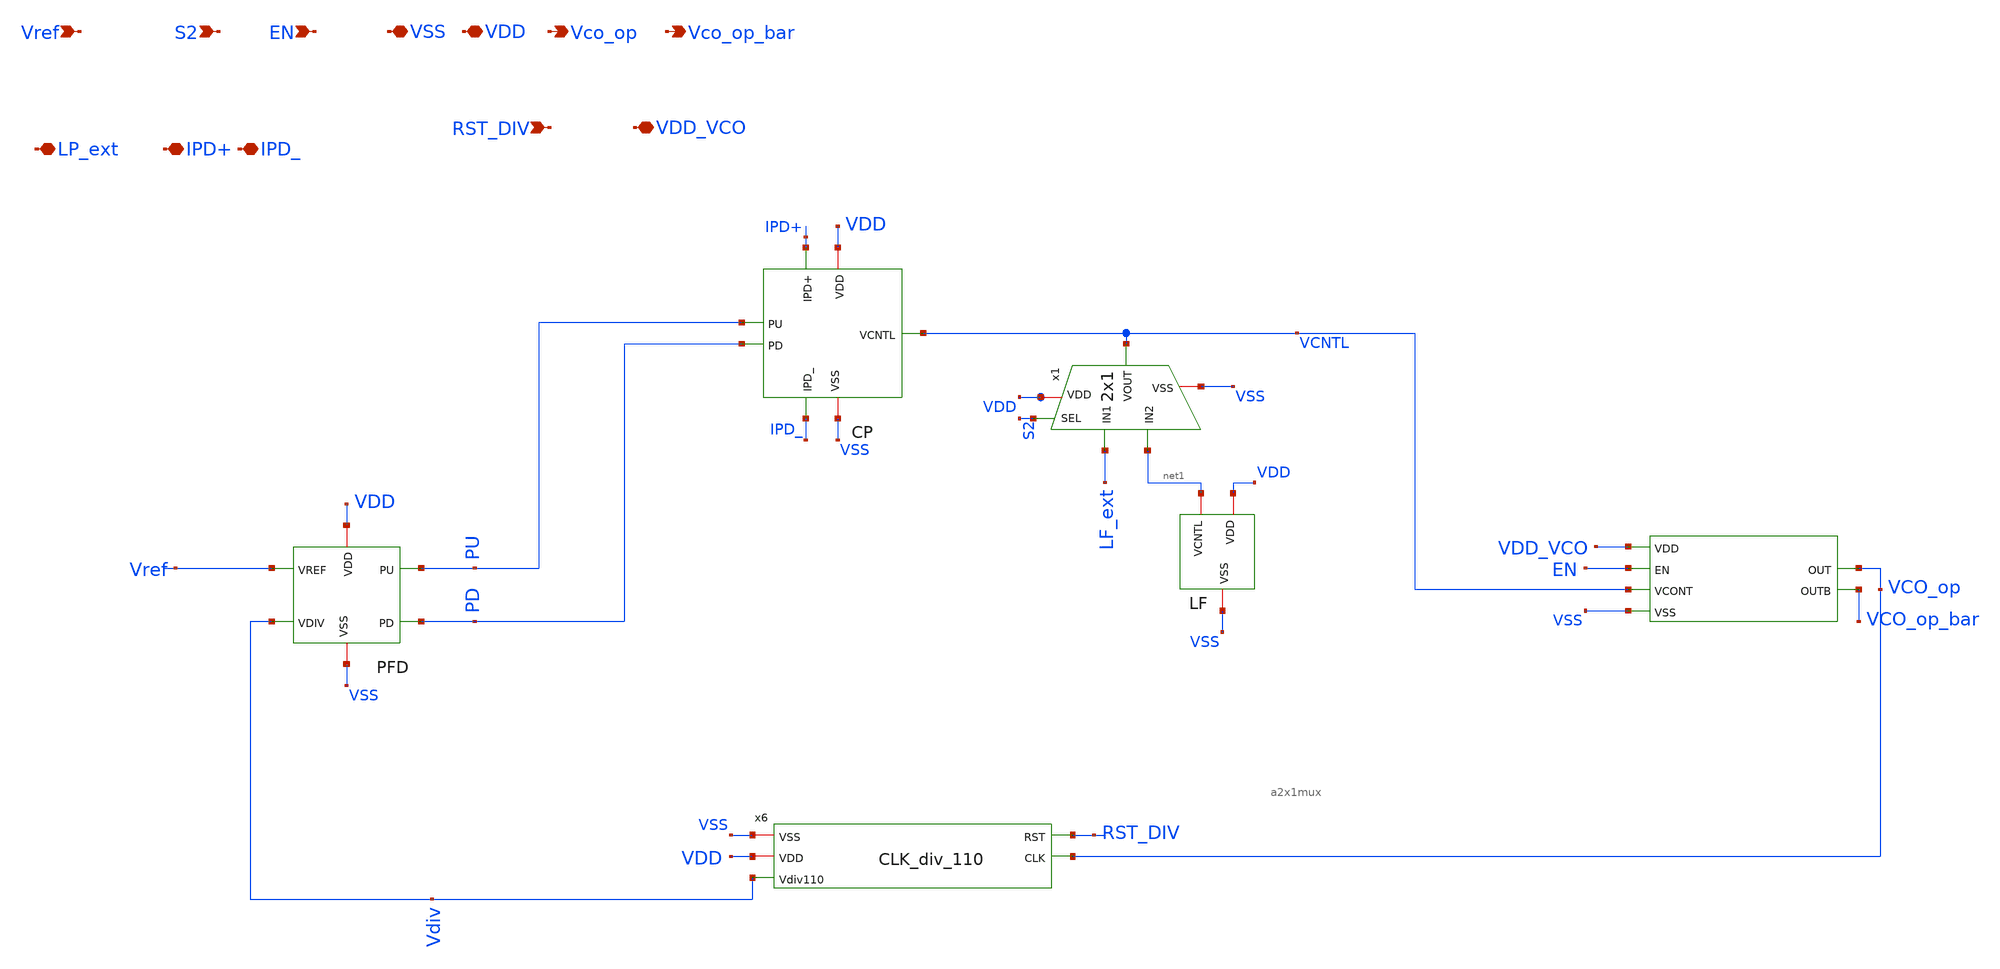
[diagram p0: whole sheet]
** sch_path: Clock_Generator_PAKISTAN_02/Schematics/pll_1_top.sch
**.subckt pll_1_top VSS VDD Vco_op S2 Vref Vco_op_bar VDD_VCO RST_DIV IPD+ IPD_ EN LP_ext
*.iopin VSS
*.iopin VDD
*.opin Vco_op
*.ipin S2
*.ipin Vref
*.opin Vco_op_bar
*.iopin VDD_VCO
*.ipin RST_DIV
*.iopin IPD+
*.iopin IPD_
*.ipin EN
*.iopin LP_ext
x3 VSS Vref Vdiv PU PD VDD PFD
x5 IPD+ IPD_ PU PD VCNTL VSS VDD CP
x1 LF_ext VDD VCNTL S2 VSS net1 a2x1mux
x4 net1 VDD VSS LF
x6 VSS VDD RST_DIV Vdiv VCO_op CLK_div_110
x2 VDD_VCO EN VCO_op VCO_op_bar VCNTL VSS VCO
**.ends
.end
